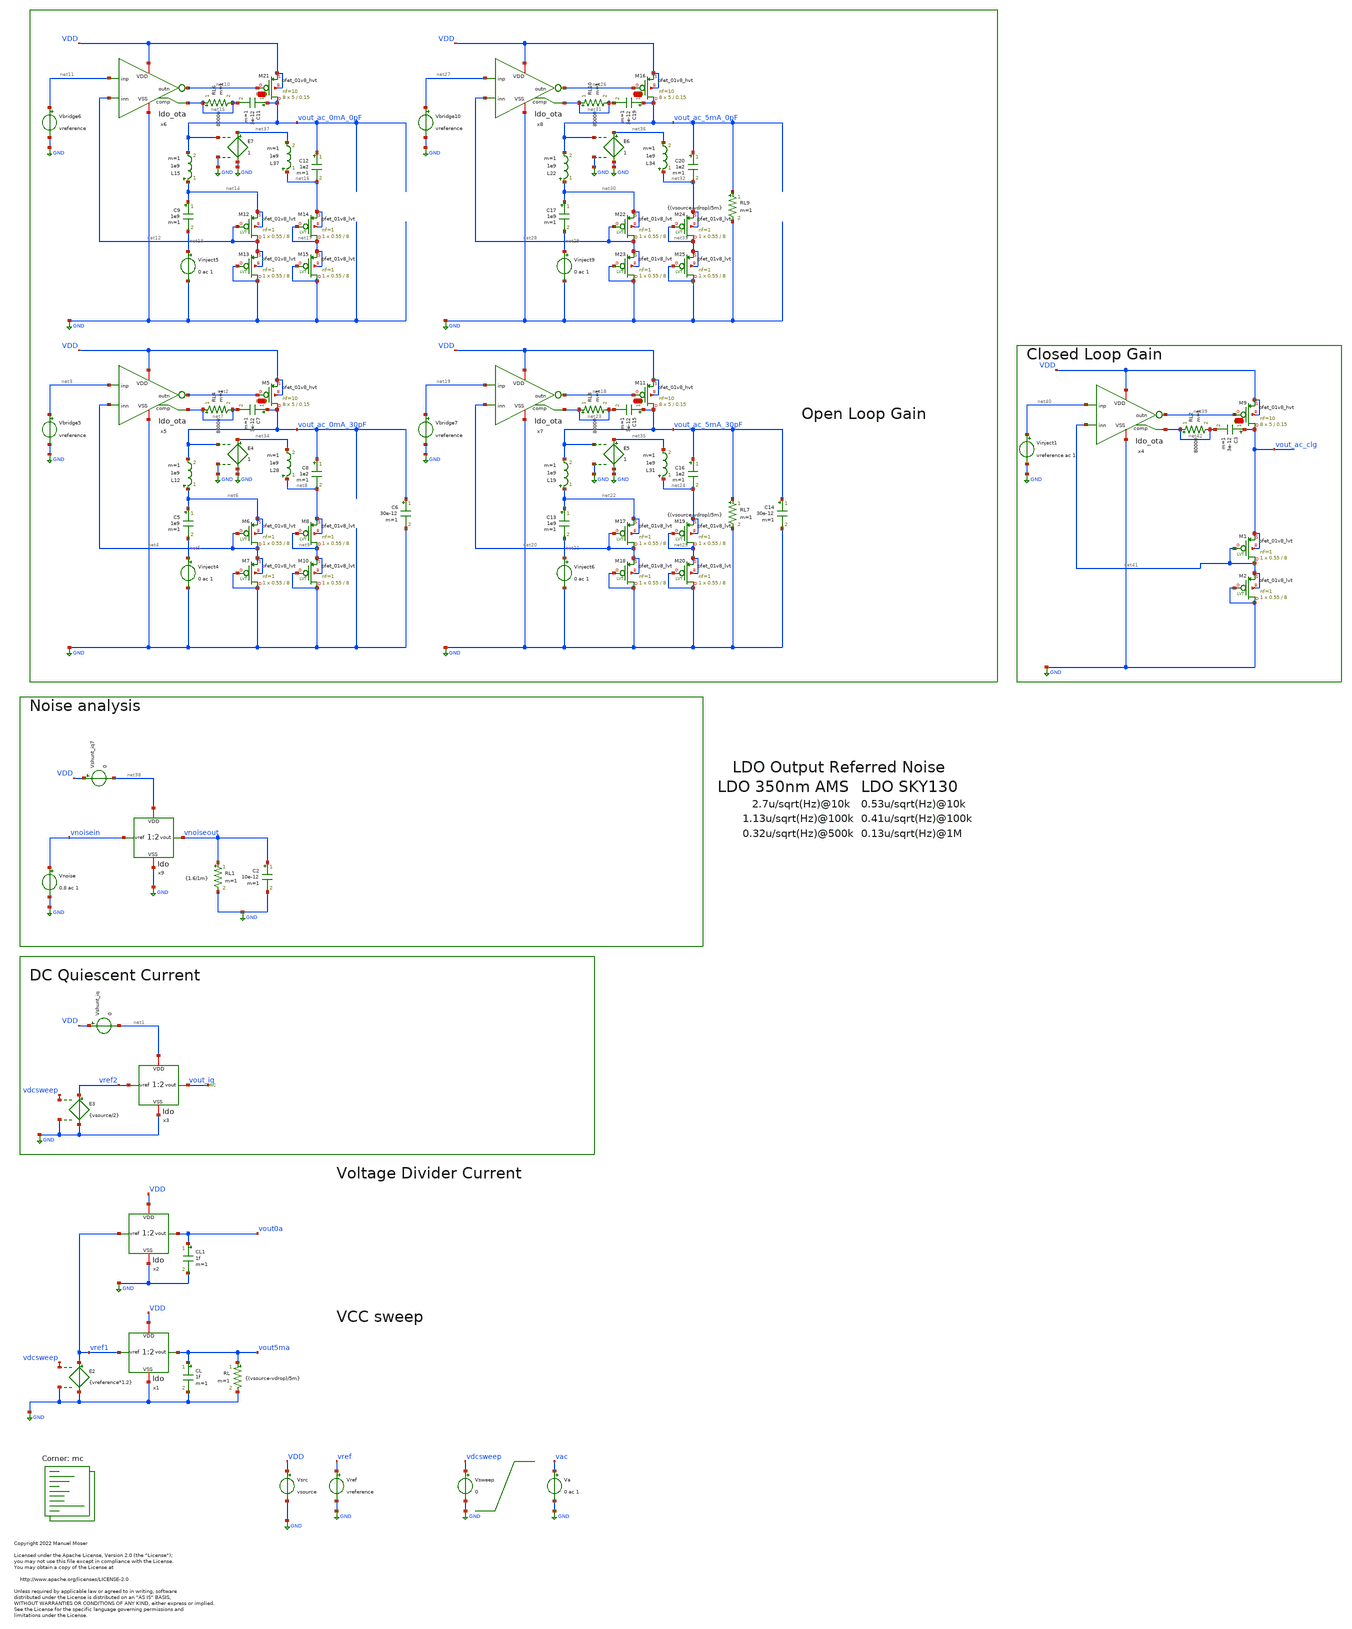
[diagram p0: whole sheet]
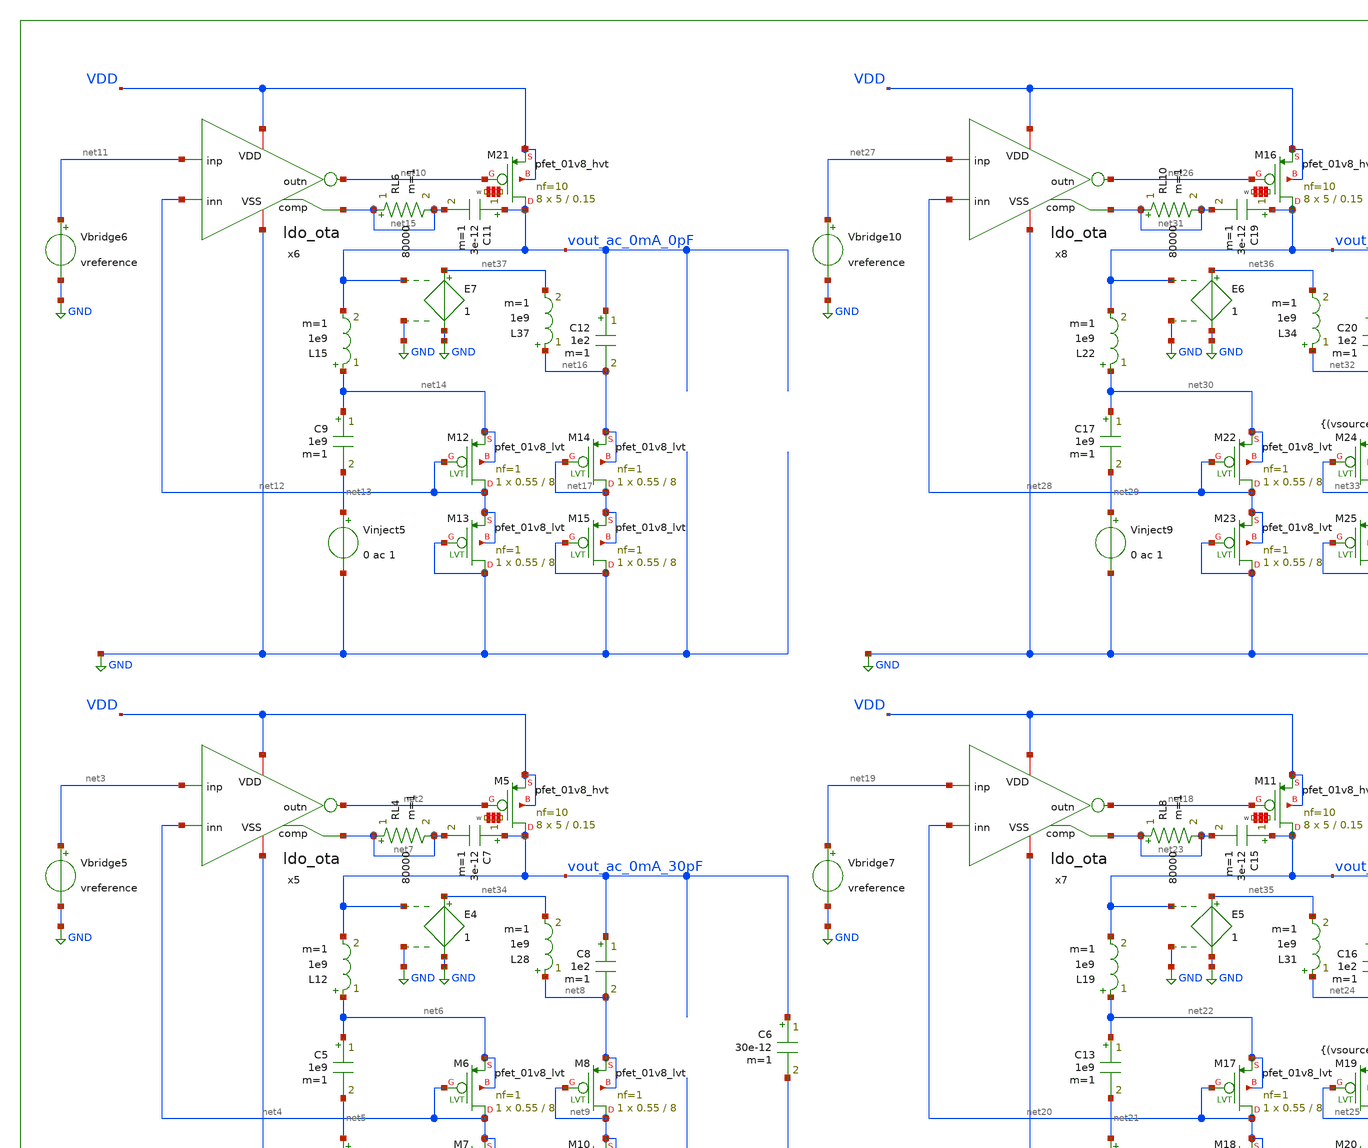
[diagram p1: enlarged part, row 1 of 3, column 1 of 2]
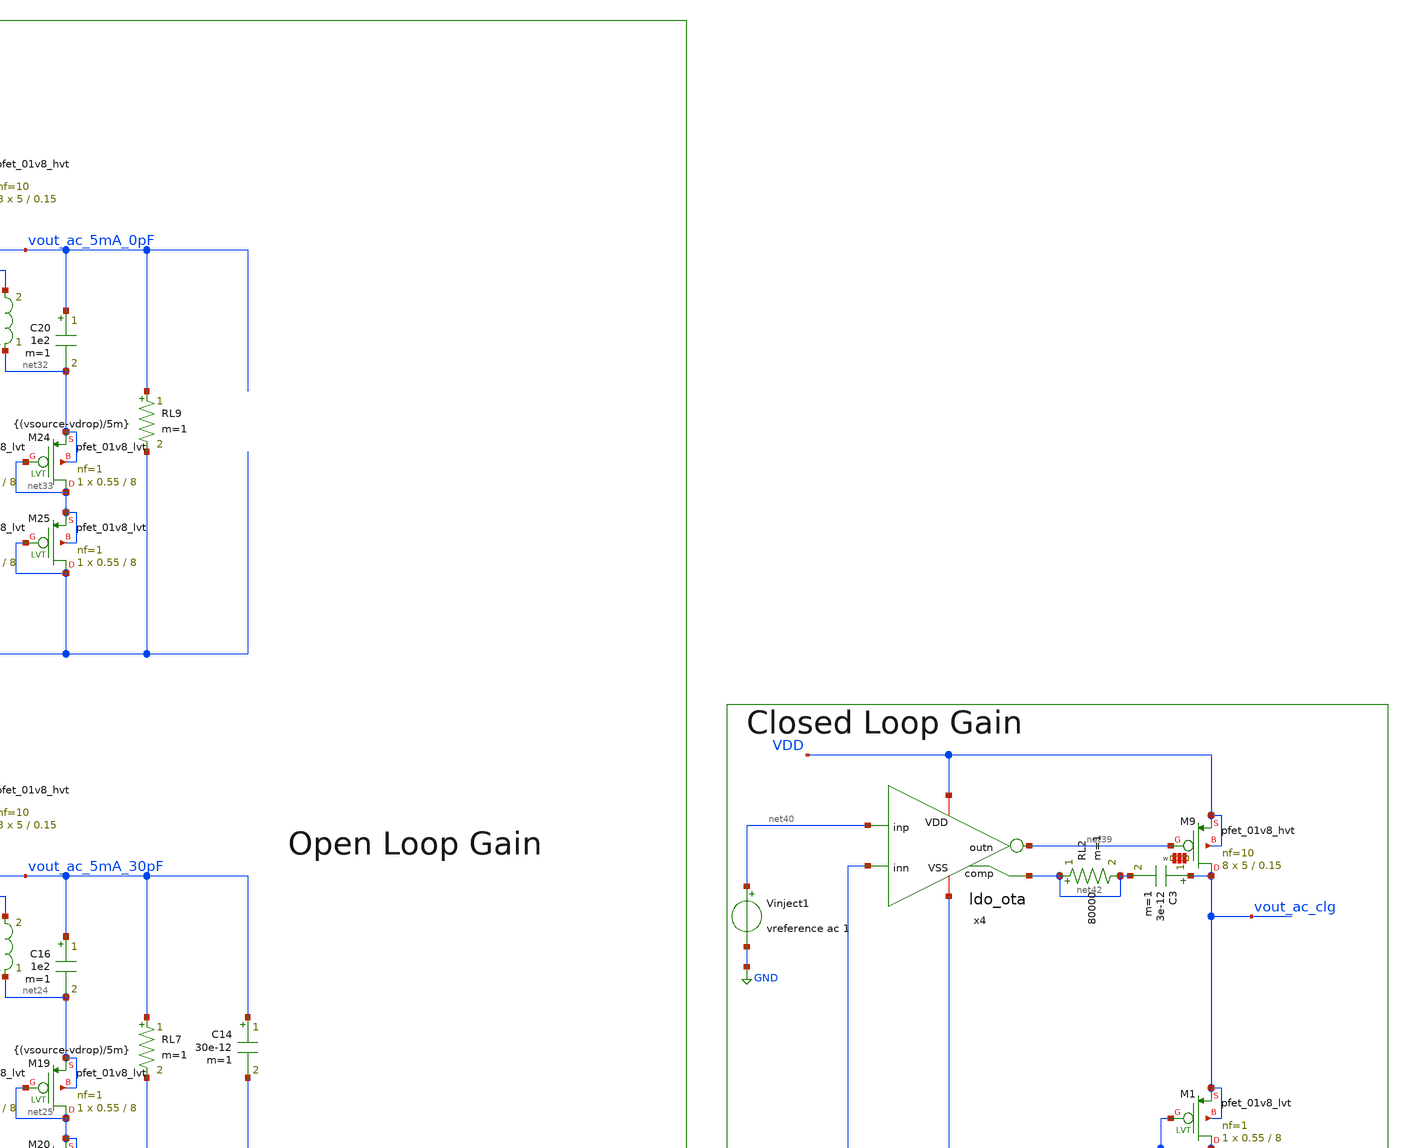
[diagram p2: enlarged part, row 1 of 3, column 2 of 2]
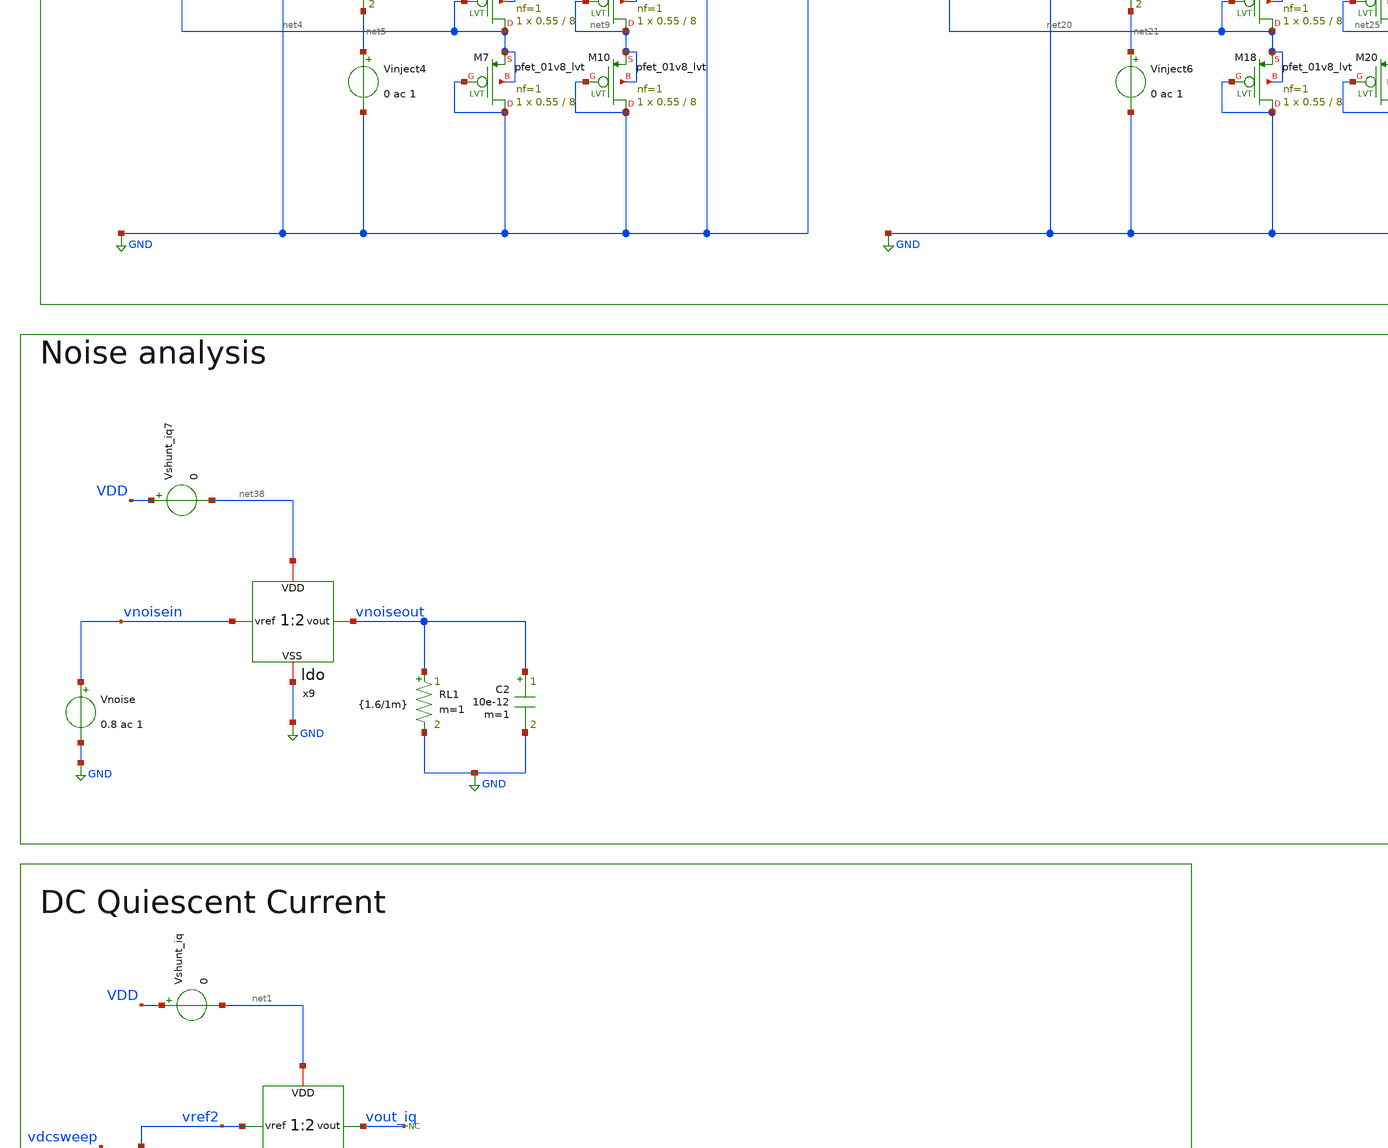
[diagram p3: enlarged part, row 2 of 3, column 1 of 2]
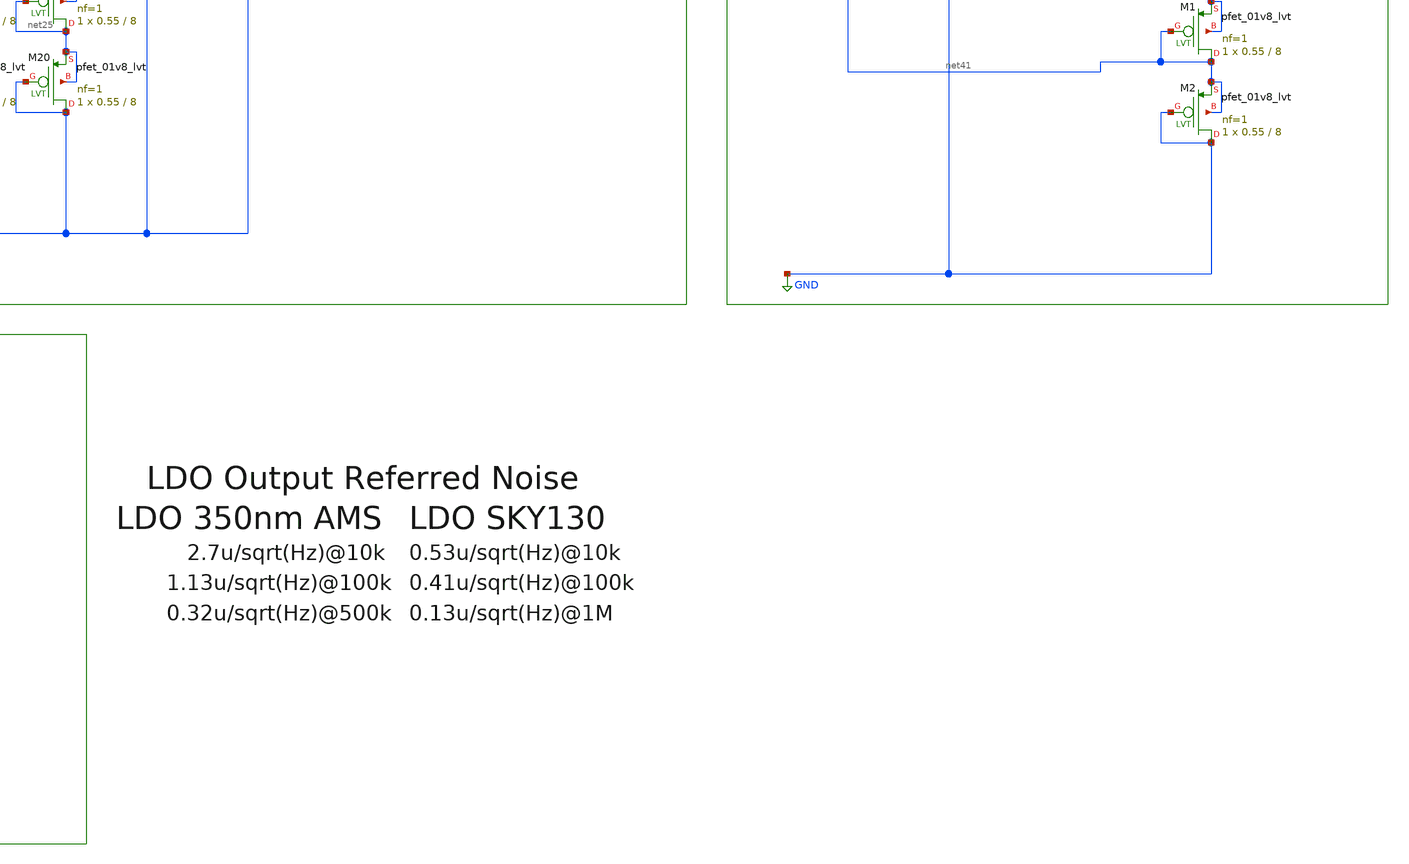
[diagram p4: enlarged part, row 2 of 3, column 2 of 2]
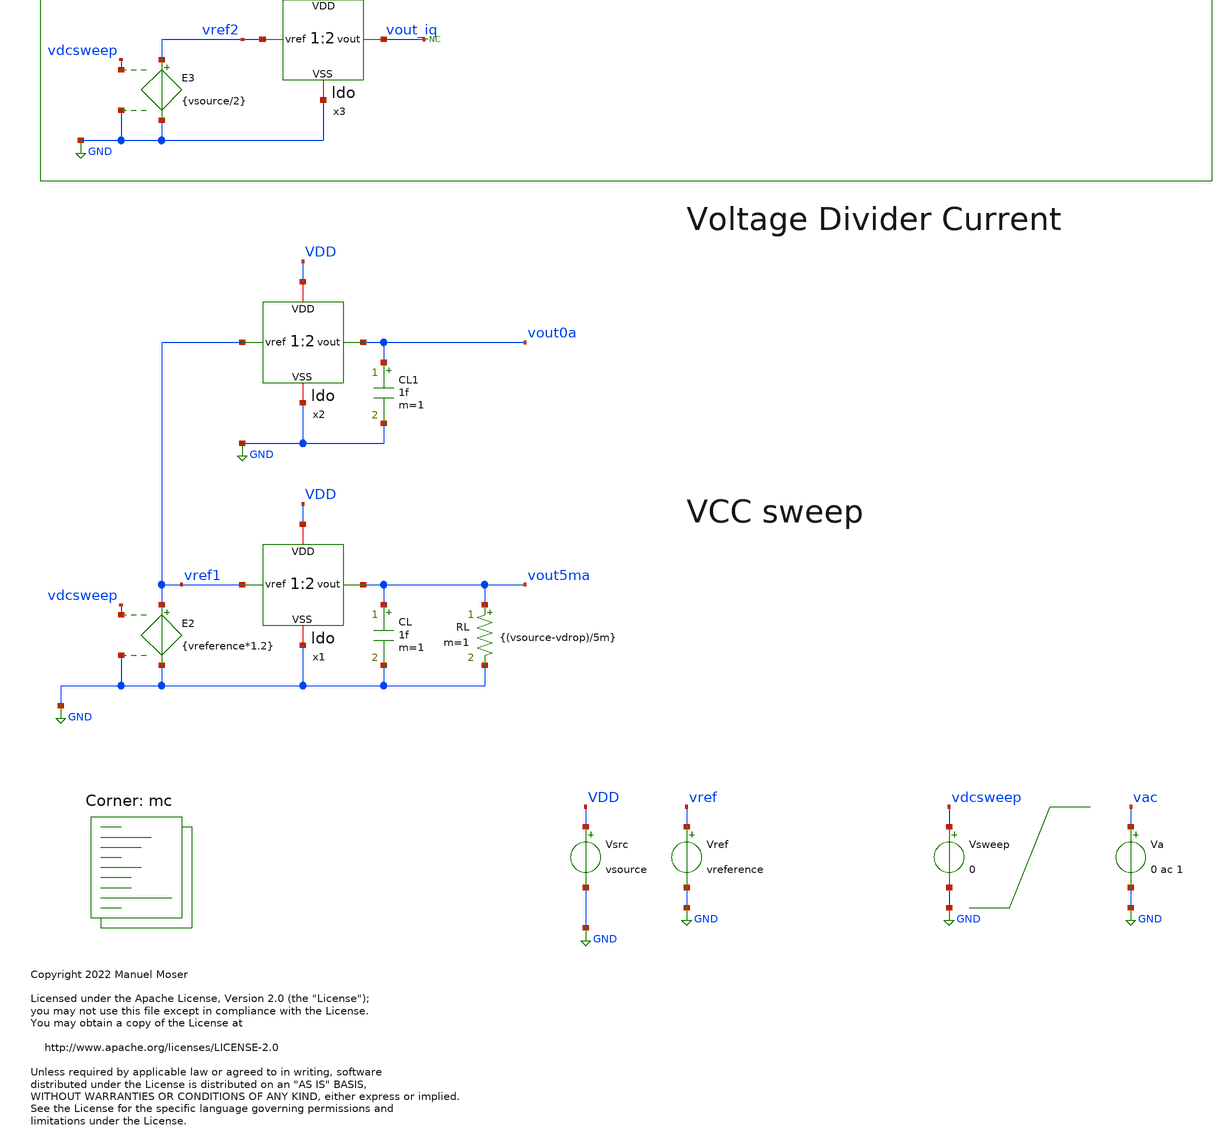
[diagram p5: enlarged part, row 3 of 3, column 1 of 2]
** sch_path: xschem/ldo_tb.sch
* Copyright 2022 Manuel Moser
* Licensed under the Apache License, Version 2.0 (the "License");
**.subckt ldo_tb
Vref vref GND vreference
Vsrc VDD GND vsource
Va vac GND 0 ac 1
CL vout5ma GND 1f m=1
RL vout5ma GND {(vsource-vdrop)/5m} m=1
x1 VDD vref1 vout5ma GND ldo
CL1 vout0a GND 1f m=1
x2 VDD vref1 vout0a GND ldo
Vsweep vdcsweep GND 0
E2 vref1 GND vdcsweep GND {vreference*1.2}
x3 net1 vref2 vout_iq GND ldo
Vshunt_iq VDD net1 0
E3 vref2 GND vdcsweep GND {vsource/2}
* noconn vout_iq
Vnoise vnoisein GND 0.8 ac 1
RL1 vnoiseout GND {1.6/1m} m=1
C2 vnoiseout GND 10e-12 m=1
x5 VDD net3 net2 net4 GND net7 ldo_ota
L12 net6 vout_ac_0mA_30pF 1e9 m=1
C5 net6 net5 1e9 m=1
Vinject4 net5 GND 0 ac 1
Vbridge5 net3 GND vreference
C6 vout_ac_0mA_30pF GND 30e-12 m=1
C7 vout_ac_0mA_30pF net7 3e-12 m=1
RL4 net7 net7 80000 m=1
XM6 net4 net4 net6 net6 sky130_fd_pr__pfet_01v8_lvt L=8 W=0.55 nf=1 ad='int((nf+1)/2) * W/nf * 0.29'
+ as='int((nf+2)/2) * W/nf * 0.29' pd='2*int((nf+1)/2) * (W/nf + 0.29)' ps='2*int((nf+2)/2) * (W/nf + 0.29)'
+ nrd='0.29 / W' nrs='0.29 / W' sa=0 sb=0 sd=0 mult=1 m=1
XM7 GND GND net4 net4 sky130_fd_pr__pfet_01v8_lvt L=8 W=0.55 nf=1 ad='int((nf+1)/2) * W/nf * 0.29' as='int((nf+2)/2) * W/nf * 0.29'
+ pd='2*int((nf+1)/2) * (W/nf + 0.29)' ps='2*int((nf+2)/2) * (W/nf + 0.29)' nrd='0.29 / W' nrs='0.29 / W'
+ sa=0 sb=0 sd=0 mult=1 m=1
XM8 net9 net9 net8 net8 sky130_fd_pr__pfet_01v8_lvt L=8 W=0.55 nf=1 ad='int((nf+1)/2) * W/nf * 0.29'
+ as='int((nf+2)/2) * W/nf * 0.29' pd='2*int((nf+1)/2) * (W/nf + 0.29)' ps='2*int((nf+2)/2) * (W/nf + 0.29)'
+ nrd='0.29 / W' nrs='0.29 / W' sa=0 sb=0 sd=0 mult=1 m=1
XM10 GND GND net9 net9 sky130_fd_pr__pfet_01v8_lvt L=8 W=0.55 nf=1 ad='int((nf+1)/2) * W/nf * 0.29' as='int((nf+2)/2) * W/nf * 0.29'
+ pd='2*int((nf+1)/2) * (W/nf + 0.29)' ps='2*int((nf+2)/2) * (W/nf + 0.29)' nrd='0.29 / W' nrs='0.29 / W'
+ sa=0 sb=0 sd=0 mult=1 m=1
C8 vout_ac_0mA_30pF net8 1e2 m=1
x6 VDD net11 net10 net12 GND net15 ldo_ota
L15 net14 vout_ac_0mA_0pF 1e9 m=1
C9 net14 net13 1e9 m=1
Vinject5 net13 GND 0 ac 1
Vbridge6 net11 GND vreference
C11 vout_ac_0mA_0pF net15 3e-12 m=1
RL6 net15 net15 80000 m=1
XM12 net12 net12 net14 net14 sky130_fd_pr__pfet_01v8_lvt L=8 W=0.55 nf=1 ad='int((nf+1)/2) * W/nf * 0.29'
+ as='int((nf+2)/2) * W/nf * 0.29' pd='2*int((nf+1)/2) * (W/nf + 0.29)' ps='2*int((nf+2)/2) * (W/nf + 0.29)'
+ nrd='0.29 / W' nrs='0.29 / W' sa=0 sb=0 sd=0 mult=1 m=1
XM13 GND GND net12 net12 sky130_fd_pr__pfet_01v8_lvt L=8 W=0.55 nf=1 ad='int((nf+1)/2) * W/nf * 0.29'
+ as='int((nf+2)/2) * W/nf * 0.29' pd='2*int((nf+1)/2) * (W/nf + 0.29)' ps='2*int((nf+2)/2) * (W/nf + 0.29)'
+ nrd='0.29 / W' nrs='0.29 / W' sa=0 sb=0 sd=0 mult=1 m=1
XM14 net17 net17 net16 net16 sky130_fd_pr__pfet_01v8_lvt L=8 W=0.55 nf=1 ad='int((nf+1)/2) * W/nf * 0.29'
+ as='int((nf+2)/2) * W/nf * 0.29' pd='2*int((nf+1)/2) * (W/nf + 0.29)' ps='2*int((nf+2)/2) * (W/nf + 0.29)'
+ nrd='0.29 / W' nrs='0.29 / W' sa=0 sb=0 sd=0 mult=1 m=1
XM15 GND GND net17 net17 sky130_fd_pr__pfet_01v8_lvt L=8 W=0.55 nf=1 ad='int((nf+1)/2) * W/nf * 0.29'
+ as='int((nf+2)/2) * W/nf * 0.29' pd='2*int((nf+1)/2) * (W/nf + 0.29)' ps='2*int((nf+2)/2) * (W/nf + 0.29)'
+ nrd='0.29 / W' nrs='0.29 / W' sa=0 sb=0 sd=0 mult=1 m=1
C12 vout_ac_0mA_0pF net16 1e2 m=1
x7 VDD net19 net18 net20 GND net23 ldo_ota
L19 net22 vout_ac_5mA_30pF 1e9 m=1
C13 net22 net21 1e9 m=1
Vinject6 net21 GND 0 ac 1
Vbridge7 net19 GND vreference
RL7 vout_ac_5mA_30pF GND {(vsource-vdrop)/5m} m=1
C14 vout_ac_5mA_30pF GND 30e-12 m=1
C15 vout_ac_5mA_30pF net23 3e-12 m=1
RL8 net23 net23 80000 m=1
XM17 net20 net20 net22 net22 sky130_fd_pr__pfet_01v8_lvt L=8 W=0.55 nf=1 ad='int((nf+1)/2) * W/nf * 0.29'
+ as='int((nf+2)/2) * W/nf * 0.29' pd='2*int((nf+1)/2) * (W/nf + 0.29)' ps='2*int((nf+2)/2) * (W/nf + 0.29)'
+ nrd='0.29 / W' nrs='0.29 / W' sa=0 sb=0 sd=0 mult=1 m=1
XM18 GND GND net20 net20 sky130_fd_pr__pfet_01v8_lvt L=8 W=0.55 nf=1 ad='int((nf+1)/2) * W/nf * 0.29'
+ as='int((nf+2)/2) * W/nf * 0.29' pd='2*int((nf+1)/2) * (W/nf + 0.29)' ps='2*int((nf+2)/2) * (W/nf + 0.29)'
+ nrd='0.29 / W' nrs='0.29 / W' sa=0 sb=0 sd=0 mult=1 m=1
XM19 net25 net25 net24 net24 sky130_fd_pr__pfet_01v8_lvt L=8 W=0.55 nf=1 ad='int((nf+1)/2) * W/nf * 0.29'
+ as='int((nf+2)/2) * W/nf * 0.29' pd='2*int((nf+1)/2) * (W/nf + 0.29)' ps='2*int((nf+2)/2) * (W/nf + 0.29)'
+ nrd='0.29 / W' nrs='0.29 / W' sa=0 sb=0 sd=0 mult=1 m=1
XM20 GND GND net25 net25 sky130_fd_pr__pfet_01v8_lvt L=8 W=0.55 nf=1 ad='int((nf+1)/2) * W/nf * 0.29'
+ as='int((nf+2)/2) * W/nf * 0.29' pd='2*int((nf+1)/2) * (W/nf + 0.29)' ps='2*int((nf+2)/2) * (W/nf + 0.29)'
+ nrd='0.29 / W' nrs='0.29 / W' sa=0 sb=0 sd=0 mult=1 m=1
C16 vout_ac_5mA_30pF net24 1e2 m=1
x8 VDD net27 net26 net28 GND net31 ldo_ota
L22 net30 vout_ac_5mA_0pF 1e9 m=1
C17 net30 net29 1e9 m=1
Vinject9 net29 GND 0 ac 1
Vbridge10 net27 GND vreference
RL9 vout_ac_5mA_0pF GND {(vsource-vdrop)/5m} m=1
C19 vout_ac_5mA_0pF net31 3e-12 m=1
RL10 net31 net31 80000 m=1
XM22 net28 net28 net30 net30 sky130_fd_pr__pfet_01v8_lvt L=8 W=0.55 nf=1 ad='int((nf+1)/2) * W/nf * 0.29'
+ as='int((nf+2)/2) * W/nf * 0.29' pd='2*int((nf+1)/2) * (W/nf + 0.29)' ps='2*int((nf+2)/2) * (W/nf + 0.29)'
+ nrd='0.29 / W' nrs='0.29 / W' sa=0 sb=0 sd=0 mult=1 m=1
XM23 GND GND net28 net28 sky130_fd_pr__pfet_01v8_lvt L=8 W=0.55 nf=1 ad='int((nf+1)/2) * W/nf * 0.29'
+ as='int((nf+2)/2) * W/nf * 0.29' pd='2*int((nf+1)/2) * (W/nf + 0.29)' ps='2*int((nf+2)/2) * (W/nf + 0.29)'
+ nrd='0.29 / W' nrs='0.29 / W' sa=0 sb=0 sd=0 mult=1 m=1
XM24 net33 net33 net32 net32 sky130_fd_pr__pfet_01v8_lvt L=8 W=0.55 nf=1 ad='int((nf+1)/2) * W/nf * 0.29'
+ as='int((nf+2)/2) * W/nf * 0.29' pd='2*int((nf+1)/2) * (W/nf + 0.29)' ps='2*int((nf+2)/2) * (W/nf + 0.29)'
+ nrd='0.29 / W' nrs='0.29 / W' sa=0 sb=0 sd=0 mult=1 m=1
XM25 GND GND net33 net33 sky130_fd_pr__pfet_01v8_lvt L=8 W=0.55 nf=1 ad='int((nf+1)/2) * W/nf * 0.29'
+ as='int((nf+2)/2) * W/nf * 0.29' pd='2*int((nf+1)/2) * (W/nf + 0.29)' ps='2*int((nf+2)/2) * (W/nf + 0.29)'
+ nrd='0.29 / W' nrs='0.29 / W' sa=0 sb=0 sd=0 mult=1 m=1
C20 vout_ac_5mA_0pF net32 1e2 m=1
L28 net8 net34 1e9 m=1
E4 net34 GND vout_ac_0mA_30pF GND 1
L31 net24 net35 1e9 m=1
E5 net35 GND vout_ac_5mA_30pF GND 1
L34 net32 net36 1e9 m=1
E6 net36 GND vout_ac_5mA_0pF GND 1
L37 net16 net37 1e9 m=1
E7 net37 GND vout_ac_0mA_0pF GND 1
XM5 vout_ac_0mA_30pF net2 VDD VDD sky130_fd_pr__pfet_01v8_hvt L=0.15 W='5 * 10 ' nf=10 ad='int((nf+1)/2) * W / nf * 0.29'
+ as='int((nf+2)/2) * W / nf * 0.29' pd='2*int((nf+1)/2) * (W / nf + 0.29)' ps='2*int((nf+2)/2) * (W / nf + 0.29)'
+ nrd='0.29 / W ' nrs='0.29 / W ' sa=0 sb=0 sd=0 mult=8 m=8
XM11 vout_ac_5mA_30pF net18 VDD VDD sky130_fd_pr__pfet_01v8_hvt L=0.15 W='5 * 10 ' nf=10 ad='int((nf+1)/2) * W / nf * 0.29'
+ as='int((nf+2)/2) * W / nf * 0.29' pd='2*int((nf+1)/2) * (W / nf + 0.29)' ps='2*int((nf+2)/2) * (W / nf + 0.29)'
+ nrd='0.29 / W ' nrs='0.29 / W ' sa=0 sb=0 sd=0 mult=8 m=8
XM16 vout_ac_5mA_0pF net26 VDD VDD sky130_fd_pr__pfet_01v8_hvt L=0.15 W='5 * 10 ' nf=10 ad='int((nf+1)/2) * W / nf * 0.29'
+ as='int((nf+2)/2) * W / nf * 0.29' pd='2*int((nf+1)/2) * (W / nf + 0.29)' ps='2*int((nf+2)/2) * (W / nf + 0.29)'
+ nrd='0.29 / W ' nrs='0.29 / W ' sa=0 sb=0 sd=0 mult=8 m=8
XM21 vout_ac_0mA_0pF net10 VDD VDD sky130_fd_pr__pfet_01v8_hvt L=0.15 W='5 * 10 ' nf=10 ad='int((nf+1)/2) * W / nf * 0.29'
+ as='int((nf+2)/2) * W / nf * 0.29' pd='2*int((nf+1)/2) * (W / nf + 0.29)' ps='2*int((nf+2)/2) * (W / nf + 0.29)'
+ nrd='0.29 / W ' nrs='0.29 / W ' sa=0 sb=0 sd=0 mult=8 m=8
x9 net38 vnoisein vnoiseout GND ldo
Vshunt_iq7 VDD net38 0
x4 VDD net40 net39 net41 GND net42 ldo_ota
C3 vout_ac_clg net42 3e-12 m=1
RL2 net42 net42 80000 m=1
XM1 net41 net41 vout_ac_clg vout_ac_clg sky130_fd_pr__pfet_01v8_lvt L=8 W=0.55 nf=1 ad='int((nf+1)/2) * W/nf * 0.29'
+ as='int((nf+2)/2) * W/nf * 0.29' pd='2*int((nf+1)/2) * (W/nf + 0.29)' ps='2*int((nf+2)/2) * (W/nf + 0.29)'
+ nrd='0.29 / W' nrs='0.29 / W' sa=0 sb=0 sd=0 mult=1 m=1
XM2 GND GND net41 net41 sky130_fd_pr__pfet_01v8_lvt L=8 W=0.55 nf=1 ad='int((nf+1)/2) * W/nf * 0.29'
+ as='int((nf+2)/2) * W/nf * 0.29' pd='2*int((nf+1)/2) * (W/nf + 0.29)' ps='2*int((nf+2)/2) * (W/nf + 0.29)'
+ nrd='0.29 / W' nrs='0.29 / W' sa=0 sb=0 sd=0 mult=1 m=1
XM9 vout_ac_clg net39 VDD VDD sky130_fd_pr__pfet_01v8_hvt L=0.15 W='5 * 10 ' nf=10 ad='int((nf+1)/2) * W / nf * 0.29'
+ as='int((nf+2)/2) * W / nf * 0.29' pd='2*int((nf+1)/2) * (W / nf + 0.29)' ps='2*int((nf+2)/2) * (W / nf + 0.29)'
+ nrd='0.29 / W ' nrs='0.29 / W ' sa=0 sb=0 sd=0 mult=8 m=8
Vinject1 net40 GND vreference ac 1
**** begin user architecture code



.temp 27
*.option gmin = 1e-16
.option RSHUNT=1E15
.option method = gear

.param vsource = 1.80
.param vdrop = 0.20
.param vreference = {(vsource-vdrop)/2}

.save all
.options savecurrents

.control
set num_threads = 12
write results_ldo.raw
set appendwrite

noise v(vnoiseout) Vnoise dec 10 1 100meg
write results_ldo.raw noise1.all noise2.all

repeat 5
reset

dc vsweep 0 1 0.01 temp -30 60 90
write results_ldo.raw   vref1 vout5ma vout0a x1.vota x1.vfb
+ @m.x1.xm9.msky130_fd_pr__pfet_01v8_lvt[id]  vref2 i(vshunt_iq)

ac dec 10 1 10meg
write results_ldo.raw vout_ac_0mA_0pF vout_ac_0mA_30pF vout_ac_5mA_0pF vout_ac_5mA_30pF vout_ac_clg

*pz vinject gnd vout_ac_gain gnd vol pz


end

.endc




.lib $::SKYWATER_MODELS/sky130.lib.spice mc
**** end user architecture code
**.ends
.GLOBAL GND
.end
